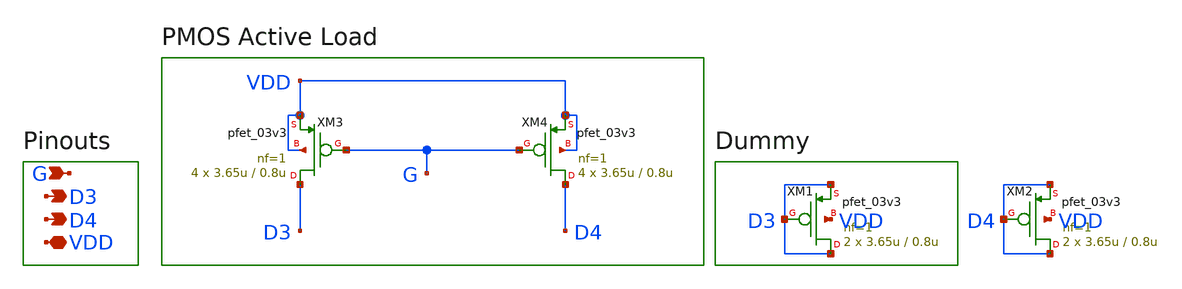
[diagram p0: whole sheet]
** sch_path: designs/libs/core_ota/active_load_diff_out/active_load_diff_out.sch
**.subckt active_load_diff_out VDD D3 D4 G
*.iopin VDD
*.opin D3
*.opin D4
*.ipin G
XM3 D3 G VDD VDD pfet_03v3 L=0.8u W=3.65u nf=1 ad='int((nf+1)/2) * W/nf * 0.18u' as='int((nf+2)/2) * W/nf * 0.18u'
+ pd='2*int((nf+1)/2) * (W/nf + 0.18u)' ps='2*int((nf+2)/2) * (W/nf + 0.18u)' nrd='0.18u / W' nrs='0.18u / W'
+ sa=0 sb=0 sd=0 m=4
XM4 D4 G VDD VDD pfet_03v3 L=0.8u W=3.65u nf=1 ad='int((nf+1)/2) * W/nf * 0.18u' as='int((nf+2)/2) * W/nf * 0.18u'
+ pd='2*int((nf+1)/2) * (W/nf + 0.18u)' ps='2*int((nf+2)/2) * (W/nf + 0.18u)' nrd='0.18u / W' nrs='0.18u / W'
+ sa=0 sb=0 sd=0 m=4
XM1 D3 D3 D3 VDD pfet_03v3 L=0.8u W=3.65u nf=1 ad='int((nf+1)/2) * W/nf * 0.18u' as='int((nf+2)/2) * W/nf * 0.18u'
+ pd='2*int((nf+1)/2) * (W/nf + 0.18u)' ps='2*int((nf+2)/2) * (W/nf + 0.18u)' nrd='0.18u / W' nrs='0.18u / W'
+ sa=0 sb=0 sd=0 m=2
XM2 D4 D4 D4 VDD pfet_03v3 L=0.8u W=3.65u nf=1 ad='int((nf+1)/2) * W/nf * 0.18u' as='int((nf+2)/2) * W/nf * 0.18u'
+ pd='2*int((nf+1)/2) * (W/nf + 0.18u)' ps='2*int((nf+2)/2) * (W/nf + 0.18u)' nrd='0.18u / W' nrs='0.18u / W'
+ sa=0 sb=0 sd=0 m=2
**.ends
.end
